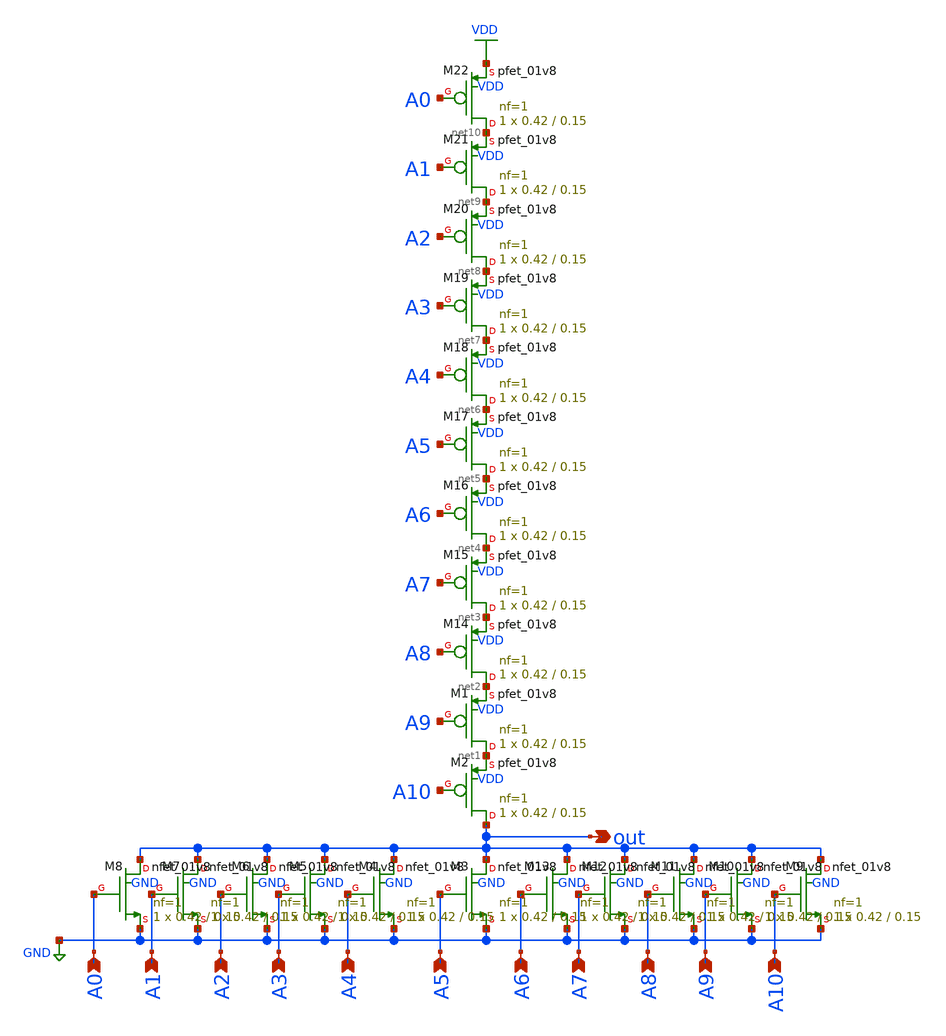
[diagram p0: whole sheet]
** sch_path: xschem/sparse_nor/sparse_nor.sch
**.subckt sparse_nor out A0 A1 A2 A3 A4 A5 A6 A7 A8 A9 A10
*.opin out
*.ipin A0
*.ipin A1
*.ipin A2
*.ipin A3
*.ipin A4
*.ipin A5
*.ipin A6
*.ipin A7
*.ipin A8
*.ipin A9
*.ipin A10
XM2 out A10 net1 VDD sky130_fd_pr__pfet_01v8 L=0.15 W=0.42 nf=1 ad='int((nf+1)/2) * W/nf * 0.29' as='int((nf+2)/2) * W/nf * 0.29'
+ pd='2*int((nf+1)/2) * (W/nf + 0.29)' ps='2*int((nf+2)/2) * (W/nf + 0.29)' nrd='0.29 / W' nrs='0.29 / W'
+ sa=0 sb=0 sd=0 mult=1 m=1
XM3 out A5 GND GND sky130_fd_pr__nfet_01v8 L=0.15 W=0.42 nf=1 ad='int((nf+1)/2) * W/nf * 0.29' as='int((nf+2)/2) * W/nf * 0.29'
+ pd='2*int((nf+1)/2) * (W/nf + 0.29)' ps='2*int((nf+2)/2) * (W/nf + 0.29)' nrd='0.29 / W' nrs='0.29 / W'
+ sa=0 sb=0 sd=0 mult=1 m=1
XM4 out A4 GND GND sky130_fd_pr__nfet_01v8 L=0.15 W=0.42 nf=1 ad='int((nf+1)/2) * W/nf * 0.29' as='int((nf+2)/2) * W/nf * 0.29'
+ pd='2*int((nf+1)/2) * (W/nf + 0.29)' ps='2*int((nf+2)/2) * (W/nf + 0.29)' nrd='0.29 / W' nrs='0.29 / W'
+ sa=0 sb=0 sd=0 mult=1 m=1
XM5 out A3 GND GND sky130_fd_pr__nfet_01v8 L=0.15 W=0.42 nf=1 ad='int((nf+1)/2) * W/nf * 0.29' as='int((nf+2)/2) * W/nf * 0.29'
+ pd='2*int((nf+1)/2) * (W/nf + 0.29)' ps='2*int((nf+2)/2) * (W/nf + 0.29)' nrd='0.29 / W' nrs='0.29 / W'
+ sa=0 sb=0 sd=0 mult=1 m=1
XM6 out A2 GND GND sky130_fd_pr__nfet_01v8 L=0.15 W=0.42 nf=1 ad='int((nf+1)/2) * W/nf * 0.29' as='int((nf+2)/2) * W/nf * 0.29'
+ pd='2*int((nf+1)/2) * (W/nf + 0.29)' ps='2*int((nf+2)/2) * (W/nf + 0.29)' nrd='0.29 / W' nrs='0.29 / W'
+ sa=0 sb=0 sd=0 mult=1 m=1
XM7 out A1 GND GND sky130_fd_pr__nfet_01v8 L=0.15 W=0.42 nf=1 ad='int((nf+1)/2) * W/nf * 0.29' as='int((nf+2)/2) * W/nf * 0.29'
+ pd='2*int((nf+1)/2) * (W/nf + 0.29)' ps='2*int((nf+2)/2) * (W/nf + 0.29)' nrd='0.29 / W' nrs='0.29 / W'
+ sa=0 sb=0 sd=0 mult=1 m=1
XM8 out A0 GND GND sky130_fd_pr__nfet_01v8 L=0.15 W=0.42 nf=1 ad='int((nf+1)/2) * W/nf * 0.29' as='int((nf+2)/2) * W/nf * 0.29'
+ pd='2*int((nf+1)/2) * (W/nf + 0.29)' ps='2*int((nf+2)/2) * (W/nf + 0.29)' nrd='0.29 / W' nrs='0.29 / W'
+ sa=0 sb=0 sd=0 mult=1 m=1
XM9 out A10 GND GND sky130_fd_pr__nfet_01v8 L=0.15 W=0.42 nf=1 ad='int((nf+1)/2) * W/nf * 0.29' as='int((nf+2)/2) * W/nf * 0.29'
+ pd='2*int((nf+1)/2) * (W/nf + 0.29)' ps='2*int((nf+2)/2) * (W/nf + 0.29)' nrd='0.29 / W' nrs='0.29 / W'
+ sa=0 sb=0 sd=0 mult=1 m=1
XM10 out A9 GND GND sky130_fd_pr__nfet_01v8 L=0.15 W=0.42 nf=1 ad='int((nf+1)/2) * W/nf * 0.29' as='int((nf+2)/2) * W/nf * 0.29'
+ pd='2*int((nf+1)/2) * (W/nf + 0.29)' ps='2*int((nf+2)/2) * (W/nf + 0.29)' nrd='0.29 / W' nrs='0.29 / W'
+ sa=0 sb=0 sd=0 mult=1 m=1
XM11 out A8 GND GND sky130_fd_pr__nfet_01v8 L=0.15 W=0.42 nf=1 ad='int((nf+1)/2) * W/nf * 0.29' as='int((nf+2)/2) * W/nf * 0.29'
+ pd='2*int((nf+1)/2) * (W/nf + 0.29)' ps='2*int((nf+2)/2) * (W/nf + 0.29)' nrd='0.29 / W' nrs='0.29 / W'
+ sa=0 sb=0 sd=0 mult=1 m=1
XM12 out A7 GND GND sky130_fd_pr__nfet_01v8 L=0.15 W=0.42 nf=1 ad='int((nf+1)/2) * W/nf * 0.29' as='int((nf+2)/2) * W/nf * 0.29'
+ pd='2*int((nf+1)/2) * (W/nf + 0.29)' ps='2*int((nf+2)/2) * (W/nf + 0.29)' nrd='0.29 / W' nrs='0.29 / W'
+ sa=0 sb=0 sd=0 mult=1 m=1
XM13 out A6 GND GND sky130_fd_pr__nfet_01v8 L=0.15 W=0.42 nf=1 ad='int((nf+1)/2) * W/nf * 0.29' as='int((nf+2)/2) * W/nf * 0.29'
+ pd='2*int((nf+1)/2) * (W/nf + 0.29)' ps='2*int((nf+2)/2) * (W/nf + 0.29)' nrd='0.29 / W' nrs='0.29 / W'
+ sa=0 sb=0 sd=0 mult=1 m=1
XM1 net1 A9 net2 VDD sky130_fd_pr__pfet_01v8 L=0.15 W=0.42 nf=1 ad='int((nf+1)/2) * W/nf * 0.29' as='int((nf+2)/2) * W/nf * 0.29'
+ pd='2*int((nf+1)/2) * (W/nf + 0.29)' ps='2*int((nf+2)/2) * (W/nf + 0.29)' nrd='0.29 / W' nrs='0.29 / W'
+ sa=0 sb=0 sd=0 mult=1 m=1
XM14 net2 A8 net3 VDD sky130_fd_pr__pfet_01v8 L=0.15 W=0.42 nf=1 ad='int((nf+1)/2) * W/nf * 0.29' as='int((nf+2)/2) * W/nf * 0.29'
+ pd='2*int((nf+1)/2) * (W/nf + 0.29)' ps='2*int((nf+2)/2) * (W/nf + 0.29)' nrd='0.29 / W' nrs='0.29 / W'
+ sa=0 sb=0 sd=0 mult=1 m=1
XM15 net3 A7 net4 VDD sky130_fd_pr__pfet_01v8 L=0.15 W=0.42 nf=1 ad='int((nf+1)/2) * W/nf * 0.29' as='int((nf+2)/2) * W/nf * 0.29'
+ pd='2*int((nf+1)/2) * (W/nf + 0.29)' ps='2*int((nf+2)/2) * (W/nf + 0.29)' nrd='0.29 / W' nrs='0.29 / W'
+ sa=0 sb=0 sd=0 mult=1 m=1
XM16 net4 A6 net5 VDD sky130_fd_pr__pfet_01v8 L=0.15 W=0.42 nf=1 ad='int((nf+1)/2) * W/nf * 0.29' as='int((nf+2)/2) * W/nf * 0.29'
+ pd='2*int((nf+1)/2) * (W/nf + 0.29)' ps='2*int((nf+2)/2) * (W/nf + 0.29)' nrd='0.29 / W' nrs='0.29 / W'
+ sa=0 sb=0 sd=0 mult=1 m=1
XM17 net5 A5 net6 VDD sky130_fd_pr__pfet_01v8 L=0.15 W=0.42 nf=1 ad='int((nf+1)/2) * W/nf * 0.29' as='int((nf+2)/2) * W/nf * 0.29'
+ pd='2*int((nf+1)/2) * (W/nf + 0.29)' ps='2*int((nf+2)/2) * (W/nf + 0.29)' nrd='0.29 / W' nrs='0.29 / W'
+ sa=0 sb=0 sd=0 mult=1 m=1
XM18 net6 A4 net7 VDD sky130_fd_pr__pfet_01v8 L=0.15 W=0.42 nf=1 ad='int((nf+1)/2) * W/nf * 0.29' as='int((nf+2)/2) * W/nf * 0.29'
+ pd='2*int((nf+1)/2) * (W/nf + 0.29)' ps='2*int((nf+2)/2) * (W/nf + 0.29)' nrd='0.29 / W' nrs='0.29 / W'
+ sa=0 sb=0 sd=0 mult=1 m=1
XM19 net7 A3 net8 VDD sky130_fd_pr__pfet_01v8 L=0.15 W=0.42 nf=1 ad='int((nf+1)/2) * W/nf * 0.29' as='int((nf+2)/2) * W/nf * 0.29'
+ pd='2*int((nf+1)/2) * (W/nf + 0.29)' ps='2*int((nf+2)/2) * (W/nf + 0.29)' nrd='0.29 / W' nrs='0.29 / W'
+ sa=0 sb=0 sd=0 mult=1 m=1
XM20 net8 A2 net9 VDD sky130_fd_pr__pfet_01v8 L=0.15 W=0.42 nf=1 ad='int((nf+1)/2) * W/nf * 0.29' as='int((nf+2)/2) * W/nf * 0.29'
+ pd='2*int((nf+1)/2) * (W/nf + 0.29)' ps='2*int((nf+2)/2) * (W/nf + 0.29)' nrd='0.29 / W' nrs='0.29 / W'
+ sa=0 sb=0 sd=0 mult=1 m=1
XM21 net9 A1 net10 VDD sky130_fd_pr__pfet_01v8 L=0.15 W=0.42 nf=1 ad='int((nf+1)/2) * W/nf * 0.29' as='int((nf+2)/2) * W/nf * 0.29'
+ pd='2*int((nf+1)/2) * (W/nf + 0.29)' ps='2*int((nf+2)/2) * (W/nf + 0.29)' nrd='0.29 / W' nrs='0.29 / W'
+ sa=0 sb=0 sd=0 mult=1 m=1
XM22 net10 A0 VDD VDD sky130_fd_pr__pfet_01v8 L=0.15 W=0.42 nf=1 ad='int((nf+1)/2) * W/nf * 0.29' as='int((nf+2)/2) * W/nf * 0.29'
+ pd='2*int((nf+1)/2) * (W/nf + 0.29)' ps='2*int((nf+2)/2) * (W/nf + 0.29)' nrd='0.29 / W' nrs='0.29 / W'
+ sa=0 sb=0 sd=0 mult=1 m=1
**.ends
.GLOBAL VDD
.GLOBAL GND
.end
